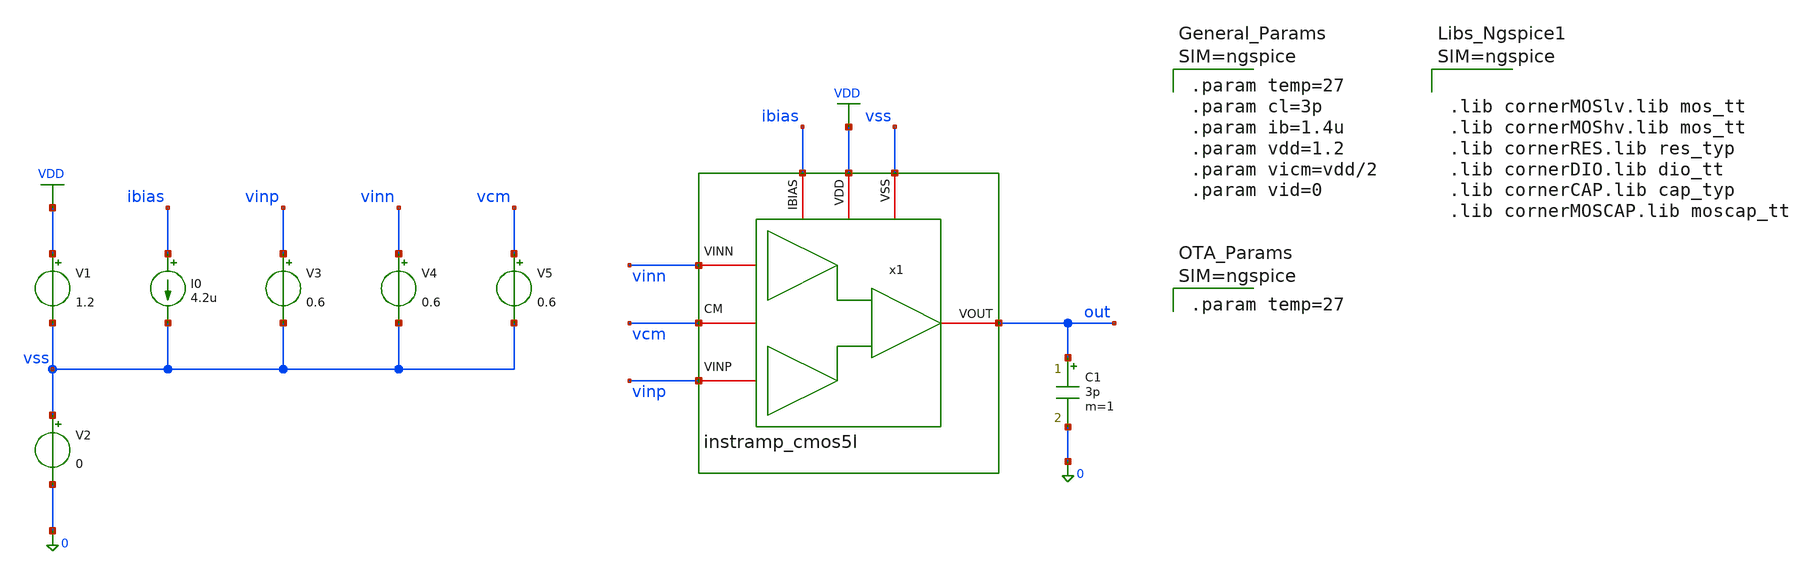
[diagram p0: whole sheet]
** sch_path: xschem/instramp_cmos5l/tb/tb_instramp_cmos5l_dc_op/tb_instramp_cmos5l_dc_op.sch
**.subckt tb_instramp_cmos5l_dc_op
C1 out 0 3p m=1
I0 ibias vss 4.2u
V1 VDD vss 1.2
V2 vss 0 0
V3 vinp vss 0.6
V4 vinn vss 0.6
x1 vss VDD ibias vinn out vinp vcm instramp_cmos5l
V5 vcm vss 0.6
**** begin user architecture code



.lib cornerMOSlv.lib mos_tt
.lib cornerMOShv.lib mos_tt
.lib cornerRES.lib res_typ
.lib cornerDIO.lib dio_tt
.lib cornerCAP.lib cap_typ
.lib cornerMOSCAP.lib moscap_tt





.param temp=27
.param cl=3p
.param ib=1.4u
.param vdd=1.2
.param vicm=vdd/2
.param vid=0





.param temp=27





.control
save all
shell mkdir -p result
op
write ./result/tb_instramp_cmos5l_dc_op.raw
show all : m, l, w, vgs, vds, vth, ids, vsat, gm, gds, fug, ids
let v_in = v(vinp)
let v_out = v(out)
let vos_mv = (v_in - v_out) * 1000
let i_q = -i(v1)
let p_q = i_q * 1.2
let p_q_uw = p_q * 1e6
let i_q_ua = i_q * 1e6
echo "======================================================="
echo " Input Common-Mode (Vin+): " $&v_in " V"
echo " Output Voltage (Vout): " $&v_out " V"
echo " Systematic Offset (Vos): " $&vos_mv " mV"
echo " Quiescent Current (I_q): " $&i_q_ua " uA"
echo " Quiescent Power (P_q): " $&p_q_uw " uW"
echo "======================================================="
.endc



**** end user architecture code
**.ends

* expanding   symbol:
*+  /foss/designs/sg13cmos5l_spma_ip__instramp/xschem/instramp_cmos5l/instramp_cmos5l.sym # of pins=7
** sym_path: /foss/designs/sg13cmos5l_spma_ip__instramp/xschem/instramp_cmos5l/instramp_cmos5l.sym
** sch_path: /foss/designs/sg13cmos5l_spma_ip__instramp/xschem/instramp_cmos5l/instramp_cmos5l.sch
.subckt instramp_cmos5l VSS VDD IBIAS VINN VOUT VINP CM
*.iopin VDD
*.iopin IBIAS
*.iopin VSS
*.iopin CM
*.iopin VOUT
*.iopin VINN
*.iopin VINP
x1 VSS IBIAS VDD net3 VINP net4 ota_cmos5l
x2 VSS IBIAS VDD net1 VINN net2 ota_cmos5l
x3 VSS IBIAS VDD net5 net6 VOUT ota_cmos5l
XR1 net4 net6 VSS rhigh w=0.5e-6 l=2e-6 m=1 b=0 mm_ok=1
XR2 net2 net5 VSS rhigh w=0.5e-6 l=2e-6 m=1 b=0 mm_ok=1
XR3 net6 CM VSS rhigh w=0.5e-6 l=8*2.23e-6 m=1 b=0 mm_ok=1
XR4 net5 VOUT VSS rhigh w=0.5e-6 l=8*2.23e-6 m=1 b=0 mm_ok=1
XR7 net2 net1 VSS rhigh w=0.5e-6 l=2e-6 m=1 b=0 mm_ok=1
XR8 net4 net3 VSS rhigh w=0.5e-6 l=2e-6 m=1 b=0 mm_ok=1
.ends


* expanding   symbol:  /foss/designs/sg13cmos5l_spma_ip__instramp/xschem/ota_cmos5l/ota_cmos5l.sym #
*+ of pins=6
** sym_path: xschem/output_buffer/ota_cmos5l.sym
** sch_path: xschem/output_buffer/ota_cmos5l.sch
.subckt ota_cmos5l VSS IBIAS VDD VINN VINP VOUT
*.iopin IBIAS
*.iopin VDD
*.iopin VSS
*.iopin VOUT
*.iopin VINP
*.iopin VINN
XM6 IBIAS IBIAS VDD VDD sg13_lv_pmos w={wbias} l={lbias} ng=1 m={m6} mm_ok=1
XM7 net1 IBIAS VDD VDD sg13_lv_pmos w={wbias} l={lbias} ng=1 m={m7} mm_ok=1
XM8 VOUT IBIAS VDD VDD sg13_lv_pmos w={wbias} l={lbias} ng=1 m={m8} mm_ok=1
XM1 net2 VINN net1 VDD sg13_lv_pmos w={winpair} l={linpair} ng=1 m=1 mm_ok=1
XM2 net3 VINP net1 VDD sg13_lv_pmos w={winpair} l={linpair} ng=1 m=1 mm_ok=1
XM3 net2 net2 VSS VSS sg13_lv_nmos w={wload} l={lload} ng=1 m=1 mm_ok=1
XM4 net3 net2 VSS VSS sg13_lv_nmos w={wload} l={lload} ng=1 m=1 mm_ok=1
XM5 VOUT net3 VSS VSS sg13_lv_nmos w={wcs} l={lcs} ng=1 m=1 mm_ok=1
XR1 net3 net4 VSS rhigh w=0.5e-6 l=1.95e-6 m=1 b=0 mm_ok=1
.save v(vinp)
.save v(vinn)
.save v(vout)
XC2 VOUT net4 cap_cmomi w=15e-6 l=15e-6 mmin=1 mmax=4 feed=double subblock=0 m=5 mm_ok=1
**** begin user architecture code


.param temp=27
.param lbias=0.15u wbias=0.15u
.param m6=1 m7=4 m8=8
.param linpair=3u winpair=20u
.param lload=5u wload=10u
.param lcs=3u wcs=20u
.param Cc=2p



**** end user architecture code
XC1 VOUT net4 cap_cmomi w=15e-6 l=15e-6 mmin=1 mmax=4 feed=double subblock=0 m=4 mm_ok=1
.ends

.GLOBAL VDD
.end
